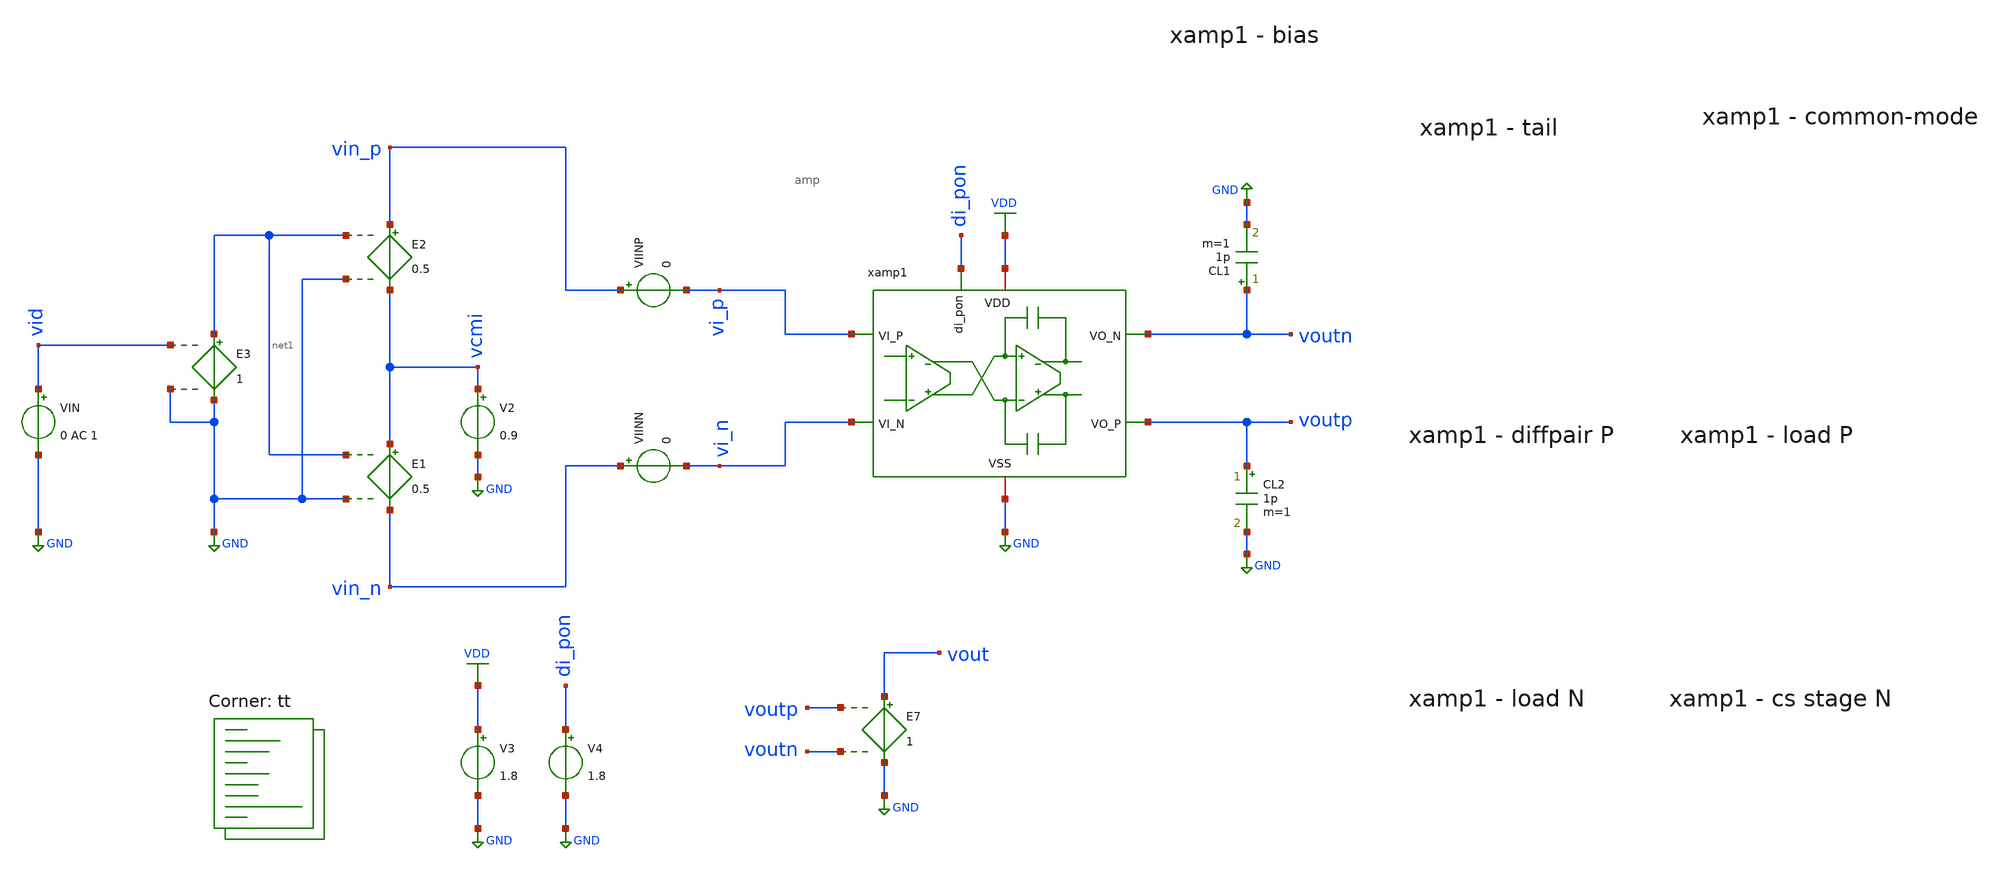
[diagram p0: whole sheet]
** sch_path: xschem/tb_amp_ol.sch
**.subckt tb_amp_ol
V3 VDD GND 1.8
V2 vcmi GND 0.9
E1 vcmi vin_n net1 GND 0.5
E2 vin_p vcmi net1 GND 0.5
VIN vid GND 0 AC 1
E3 net1 GND vid GND 1
VIINP vin_p vi_p 0
VIINN vin_n vi_n 0
V4 di_pon GND 1.8
E7 vout GND voutp voutn 1
CL2 voutp GND 1p m=1
xamp1 VDD vi_n vi_p voutp di_pon voutn GND amp
CL1 voutn GND 1p m=1
**** begin user architecture code
.lib $::SKYWATER_MODELS/sky130.lib.spice tt


.include /foss/designs/amp_dev_sav.spice
.options savecurrents

.save all
.control
set doAmpSim = 1

if $doAmpSim eq 1
	setplot const
	let f_min = 10
	let f_max = 1G
	let f_stop = 500k

	let Adc = 220
	let v_step_o = 0.9
	let v_step_i = -v_step_o/Adc

	let t_rf = 0.01u
	let t_step = 5u
	let t_delay = 0
	let t_per = 2*t_step

	let tstep = 0.001*t_step
	let tstop = 2*t_per
	let tstart = t_delay

	alter @VIN[DC] = 0.0
	alter @VIN[PULSE] = [ 0 $&v_step_i $&t_delay $&t_rf $&t_rf $&t_step $&t_per 0 ]

	ac dec 100 $&const.f_min $&const.f_max

	noise v(vout) vin dec 100 $&const.f_min $&const.f_max

	tran $&tstep $&tstop $&tstart

	setplot ac1
	let Atot = v(vout)/v(vid)

	let Amag_ol_dB = vdb(Atot)
	let Aarg_ol = 180/PI*cphase(Atot)

	**let Amag_ol_dB_1 = vdb(A1)
	**let Aarg_ol_1 = 180/PI*cphase(A1)

	**let Amag_ol_dB_2 = vdb(A2)
	**let Aarg_ol_2 = 180/PI*cphase(A2)

	meas ac Adc_ol_dB max Amag_ol_dB
	let Amag_fc = Adc_ol_dB-3

	meas ac fc find frequency when Amag_ol_dB = Amag_fc
	meas ac fug_ol find frequency when Amag_ol_dB=0
	meas ac pm find Aarg_ol when frequency=fug_ol
	let pm = 180 + pm
	print pm

	let Adc_ol_lin = 10^(Adc_ol_dB/20)
	let err_gain = 1-Adc_ol_lin/(1+Adc_ol_lin)
	print err_gain*100

	plot Amag_ol_dB Aarg_ol ylabel 'Open Loop Magnitude, Phase'

	setplot noise1
	let acgain = onoise_spectrum/inoise_spectrum
	plot onoise_spectrum ylog xlog ylabel 'Output Noise'
	*plot acgain

	setplot noise2
	print onoise_total

	setplot tran2
	let vcmo = (v(voutp)+v(voutn))/2
	plot v(vin_p) v(vin_n) v(voutp) v(voutn) vcmo
end

reset
op


*rm /foss/designs/filter/dc.txt
*show >> /foss/designs/filter/dc.txt
remzerovec
write tb_amp_ol.raw
.endc

**** end user architecture code
**.ends

* expanding   symbol:  /foss/designs/xschem/amp.sym # of pins=7
** sym_path: xschem/amp.sym
** sch_path: xschem/amp.sch
.subckt amp VDD VI_N VI_P VO_P di_pon VO_N VSS
*.iopin VSS
*.iopin VDD
*.ipin VI_P
*.ipin di_pon
*.ipin VI_N
*.opin VO_P
*.opin VO_N
XMP1 vbp vbp VDD VDD sky130_fd_pr__pfet_01v8 L=0.25 W='5 * 2 ' nf=2 ad='int((nf+1)/2) * W / nf * 0.29'
+ as='int((nf+2)/2) * W / nf * 0.29' pd='2*int((nf+1)/2) * (W / nf + 0.29)' ps='2*int((nf+2)/2) * (W / nf + 0.29)'
+ nrd='0.29 / W ' nrs='0.29 / W ' sa=0 sb=0 sd=0 mult=1 m=1
XMPSW3 vbp pon VDD VDD sky130_fd_pr__pfet_01v8 L=0.15 W='5 * 5 ' nf=5 ad='int((nf+1)/2) * W / nf * 0.29'
+ as='int((nf+2)/2) * W / nf * 0.29' pd='2*int((nf+1)/2) * (W / nf + 0.29)' ps='2*int((nf+2)/2) * (W / nf + 0.29)'
+ nrd='0.29 / W ' nrs='0.29 / W ' sa=0 sb=0 sd=0 mult=1 m=1
XMNSW1 pon_b di_pon VSS VSS sky130_fd_pr__nfet_01v8 L=0.15 W='3 * 1 ' nf=1 ad='int((nf+1)/2) * W / nf * 0.29'
+ as='int((nf+2)/2) * W / nf * 0.29' pd='2*int((nf+1)/2) * (W / nf + 0.29)' ps='2*int((nf+2)/2) * (W / nf + 0.29)'
+ nrd='0.29 / W ' nrs='0.29 / W ' sa=0 sb=0 sd=0 mult=1 m=1
XMPSW1 pon_b di_pon VDD VDD sky130_fd_pr__pfet_01v8 L=0.15 W='5 * 1 ' nf=1 ad='int((nf+1)/2) * W / nf * 0.29'
+ as='int((nf+2)/2) * W / nf * 0.29' pd='2*int((nf+1)/2) * (W / nf + 0.29)' ps='2*int((nf+2)/2) * (W / nf + 0.29)'
+ nrd='0.29 / W ' nrs='0.29 / W ' sa=0 sb=0 sd=0 mult=1 m=1
XMNSW2 pon pon_b VSS VSS sky130_fd_pr__nfet_01v8 L=0.15 W='3 * 3 ' nf=3 ad='int((nf+1)/2) * W / nf * 0.29'
+ as='int((nf+2)/2) * W / nf * 0.29' pd='2*int((nf+1)/2) * (W / nf + 0.29)' ps='2*int((nf+2)/2) * (W / nf + 0.29)'
+ nrd='0.29 / W ' nrs='0.29 / W ' sa=0 sb=0 sd=0 mult=1 m=1
XMPSW2 pon pon_b VDD VDD sky130_fd_pr__pfet_01v8 L=0.15 W='5 * 3 ' nf=3 ad='int((nf+1)/2) * W / nf * 0.29'
+ as='int((nf+2)/2) * W / nf * 0.29' pd='2*int((nf+1)/2) * (W / nf + 0.29)' ps='2*int((nf+2)/2) * (W / nf + 0.29)'
+ nrd='0.29 / W ' nrs='0.29 / W ' sa=0 sb=0 sd=0 mult=1 m=1
XMP2 viref1 vbp VDD VDD sky130_fd_pr__pfet_01v8 L=0.25 W='5 * 20 ' nf=20 ad='int((nf+1)/2) * W / nf * 0.29'
+ as='int((nf+2)/2) * W / nf * 0.29' pd='2*int((nf+1)/2) * (W / nf + 0.29)' ps='2*int((nf+2)/2) * (W / nf + 0.29)'
+ nrd='0.29 / W ' nrs='0.29 / W ' sa=0 sb=0 sd=0 mult=1 m=1
XC5 VDD vbp sky130_fd_pr__cap_mim_m3_1 W=5 L=5 MF=5 m=5
XMP4 vo1_n VI_P viref1 viref1 sky130_fd_pr__pfet_01v8 L=0.15 W='5 * 70 ' nf=70 ad='int((nf+1)/2) * W / nf * 0.29'
+ as='int((nf+2)/2) * W / nf * 0.29' pd='2*int((nf+1)/2) * (W / nf + 0.29)' ps='2*int((nf+2)/2) * (W / nf + 0.29)'
+ nrd='0.29 / W ' nrs='0.29 / W ' sa=0 sb=0 sd=0 mult=1 m=1
XMP5 vo1_p VI_N viref1 viref1 sky130_fd_pr__pfet_01v8 L=0.15 W='5 * 70 ' nf=70 ad='int((nf+1)/2) * W / nf * 0.29'
+ as='int((nf+2)/2) * W / nf * 0.29' pd='2*int((nf+1)/2) * (W / nf + 0.29)' ps='2*int((nf+2)/2) * (W / nf + 0.29)'
+ nrd='0.29 / W ' nrs='0.29 / W ' sa=0 sb=0 sd=0 mult=1 m=1
XMN1 vo1_n vfb1 VSS VSS sky130_fd_pr__nfet_01v8 L=1 W='3 * 6 ' nf=6 ad='int((nf+1)/2) * W / nf * 0.29'
+ as='int((nf+2)/2) * W / nf * 0.29' pd='2*int((nf+1)/2) * (W / nf + 0.29)' ps='2*int((nf+2)/2) * (W / nf + 0.29)'
+ nrd='0.29 / W ' nrs='0.29 / W ' sa=0 sb=0 sd=0 mult=1 m=1
XMN2 vo1_p vfb1 VSS VSS sky130_fd_pr__nfet_01v8 L=1 W='3 * 6 ' nf=6 ad='int((nf+1)/2) * W / nf * 0.29'
+ as='int((nf+2)/2) * W / nf * 0.29' pd='2*int((nf+1)/2) * (W / nf + 0.29)' ps='2*int((nf+2)/2) * (W / nf + 0.29)'
+ nrd='0.29 / W ' nrs='0.29 / W ' sa=0 sb=0 sd=0 mult=1 m=1
XC1 vo1_n vfb1 sky130_fd_pr__cap_mim_m3_1 W=5 L=5 MF=5 m=5
XC2 vfb1 vo1_p sky130_fd_pr__cap_mim_m3_1 W=5 L=5 MF=5 m=5
XMN3 VO_N vo1_p VSS VSS sky130_fd_pr__nfet_01v8 L=0.5 W='3 * 20 ' nf=20 ad='int((nf+1)/2) * W / nf * 0.29'
+ as='int((nf+2)/2) * W / nf * 0.29' pd='2*int((nf+1)/2) * (W / nf + 0.29)' ps='2*int((nf+2)/2) * (W / nf + 0.29)'
+ nrd='0.29 / W ' nrs='0.29 / W ' sa=0 sb=0 sd=0 mult=1 m=1
XMN4 VO_P vo1_n VSS VSS sky130_fd_pr__nfet_01v8 L=0.5 W='3 * 20 ' nf=20 ad='int((nf+1)/2) * W / nf * 0.29'
+ as='int((nf+2)/2) * W / nf * 0.29' pd='2*int((nf+1)/2) * (W / nf + 0.29)' ps='2*int((nf+2)/2) * (W / nf + 0.29)'
+ nrd='0.29 / W ' nrs='0.29 / W ' sa=0 sb=0 sd=0 mult=1 m=1
XMP3 vbncm vbp VDD VDD sky130_fd_pr__pfet_01v8 L=0.25 W='5 * 2 ' nf=2 ad='int((nf+1)/2) * W / nf * 0.29'
+ as='int((nf+2)/2) * W / nf * 0.29' pd='2*int((nf+1)/2) * (W / nf + 0.29)' ps='2*int((nf+2)/2) * (W / nf + 0.29)'
+ nrd='0.29 / W ' nrs='0.29 / W ' sa=0 sb=0 sd=0 mult=1 m=1
XMP6 VO_P vfb2 VDD VDD sky130_fd_pr__pfet_01v8 L=0.5 W='5 * 5 ' nf=5 ad='int((nf+1)/2) * W / nf * 0.29'
+ as='int((nf+2)/2) * W / nf * 0.29' pd='2*int((nf+1)/2) * (W / nf + 0.29)' ps='2*int((nf+2)/2) * (W / nf + 0.29)'
+ nrd='0.29 / W ' nrs='0.29 / W ' sa=0 sb=0 sd=0 mult=1 m=1
XMP7 VO_N vfb2 VDD VDD sky130_fd_pr__pfet_01v8 L=0.5 W='5 * 5 ' nf=5 ad='int((nf+1)/2) * W / nf * 0.29'
+ as='int((nf+2)/2) * W / nf * 0.29' pd='2*int((nf+1)/2) * (W / nf + 0.29)' ps='2*int((nf+2)/2) * (W / nf + 0.29)'
+ nrd='0.29 / W ' nrs='0.29 / W ' sa=0 sb=0 sd=0 mult=1 m=1
XC3 VO_N vfb2 sky130_fd_pr__cap_mim_m3_1 W=5 L=5 MF=5 m=5
XC4 vfb2 VO_P sky130_fd_pr__cap_mim_m3_1 W=5 L=5 MF=5 m=5
XMN5 vbncm vbncm VSS VSS sky130_fd_pr__nfet_01v8 L=0.5 W='3 * 5 ' nf=5 ad='int((nf+1)/2) * W / nf * 0.29'
+ as='int((nf+2)/2) * W / nf * 0.29' pd='2*int((nf+1)/2) * (W / nf + 0.29)' ps='2*int((nf+2)/2) * (W / nf + 0.29)'
+ nrd='0.29 / W ' nrs='0.29 / W ' sa=0 sb=0 sd=0 mult=1 m=1
XMN6 vfb2 vbncm VSS VSS sky130_fd_pr__nfet_01v8 L=0.5 W='3 * 4 ' nf=4 ad='int((nf+1)/2) * W / nf * 0.29'
+ as='int((nf+2)/2) * W / nf * 0.29' pd='2*int((nf+1)/2) * (W / nf + 0.29)' ps='2*int((nf+2)/2) * (W / nf + 0.29)'
+ nrd='0.29 / W ' nrs='0.29 / W ' sa=0 sb=0 sd=0 mult=1 m=1
XMNSW3 vrref_sw pon VSS VSS sky130_fd_pr__nfet_01v8 L=0.15 W='3 * 5 ' nf=5 ad='int((nf+1)/2) * W / nf * 0.29'
+ as='int((nf+2)/2) * W / nf * 0.29' pd='2*int((nf+1)/2) * (W / nf + 0.29)' ps='2*int((nf+2)/2) * (W / nf + 0.29)'
+ nrd='0.29 / W ' nrs='0.29 / W ' sa=0 sb=0 sd=0 mult=1 m=1
XRREF vrref_sw vbp VSS sky130_fd_pr__res_xhigh_po_0p35 L=5.6 mult=1 m=1
xr1 vfb1 vo1_n vo1_p VSS rstring_cm
xr2 vfb2 VO_P VO_N VSS rstring_cm
XC6 vo1_p VO_N sky130_fd_pr__cap_mim_m3_1 W=5 L=5 MF=16 m=16
XC7 vo1_n VO_P sky130_fd_pr__cap_mim_m3_1 W=5 L=5 MF=16 m=16
.ends


* expanding   symbol:  /foss/designs/xschem/rstring_cm.sym # of pins=4
** sym_path: xschem/rstring_cm.sym
** sch_path: xschem/rstring_cm.sch
.subckt rstring_cm VR_M VR_N VR_P VSS
*.iopin VSS
*.ipin VR_P
*.ipin VR_N
*.opin VR_M
XR1 VR_P net1 VSS sky130_fd_pr__res_xhigh_po_0p35 L=5.6 mult=1 m=1
XR2 net1 VR_M VSS sky130_fd_pr__res_xhigh_po_0p35 L=5.6 mult=1 m=1
XR3 VR_M net2 VSS sky130_fd_pr__res_xhigh_po_0p35 L=5.6 mult=1 m=1
XR4 net2 VR_N VSS sky130_fd_pr__res_xhigh_po_0p35 L=5.6 mult=1 m=1
.ends

.GLOBAL GND
.GLOBAL VDD
.end
